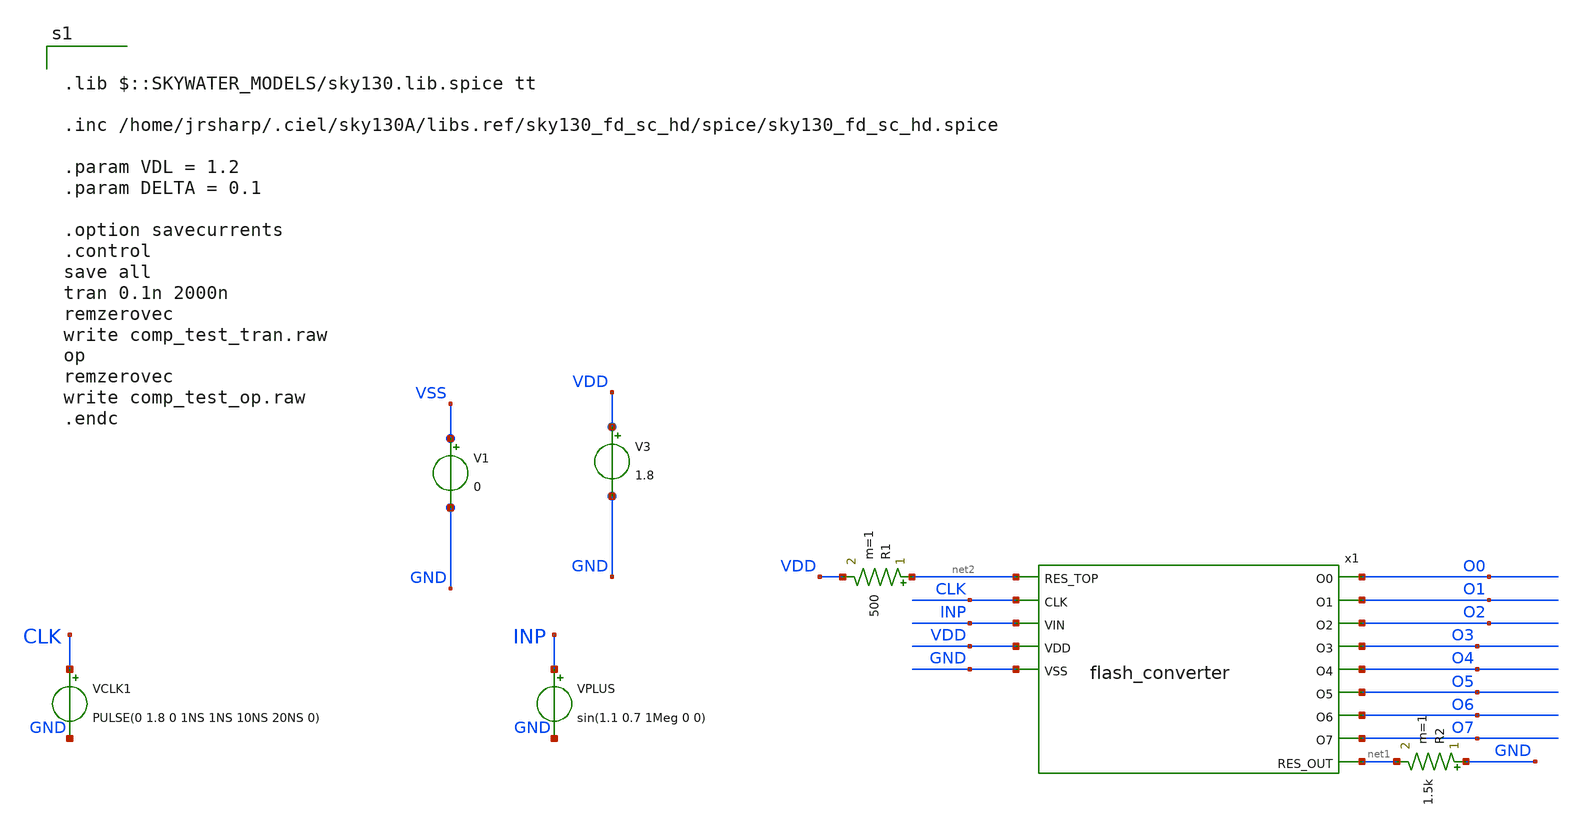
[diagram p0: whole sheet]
** sch_path: xschem/flash_converter/flash_converter_test.sch
**.subckt flash_converter_test
VPLUS INP GND sin(1.1 0.7 1Meg 0 0)
VCLK1 CLK GND PULSE(0 1.8 0 1NS 1NS 10NS 20NS 0)
R1 net2 VDD 500 m=1
R2 GND net1 1.5k m=1
V3 VDD GND 1.8
x1 net2 CLK INP O0 O1 VDD GND O2 O3 O4 O5 O6 O7 net1 flash_converter
V1 VSS GND 0
**** begin user architecture code

.lib $::SKYWATER_MODELS/sky130.lib.spice tt

.inc /home/jrsharp/.ciel/sky130A/libs.ref/sky130_fd_sc_hd/spice/sky130_fd_sc_hd.spice

.param VDL = 1.2
.param DELTA = 0.1

.option savecurrents
.control
save all
tran 0.1n 2000n
remzerovec
write comp_test_tran.raw
op
remzerovec
write comp_test_op.raw
.endc



**** end user architecture code
**.ends

* expanding   symbol:  flash_converter.sym # of pins=14
** sym_path: xschem/flash_converter/flash_converter.sym
** sch_path: xschem/flash_converter/flash_converter.sch
.subckt flash_converter RES_TOP CLK VIN O0 O1 VDD VSS O2 O3 O4 O5 O6 O7 RES_OUT
*.ipin VIN
*.ipin RES_TOP
*.opin RES_OUT
*.opin O0
*.opin O1
*.opin O2
*.opin O3
*.opin O4
*.opin O5
*.opin O6
*.opin O7
*.ipin CLK
*.ipin VDD
*.ipin VSS
x1 CLK VIN RES_TOP VDD O0 VSS high_speed_comp_top
x2 CLK VIN net1 VDD O1 VSS high_speed_comp_top
x3 CLK VIN net2 VDD O2 VSS high_speed_comp_top
x4 CLK VIN net3 VDD O3 VSS high_speed_comp_top
x5 CLK VIN net4 VDD O4 VSS high_speed_comp_top
x6 CLK VIN net5 VDD O5 VSS high_speed_comp_top
x7 CLK VIN net6 VDD O6 VSS high_speed_comp_top
x8 CLK VIN net7 VDD O7 VSS high_speed_comp_top
XR1 net1 RES_TOP VSS sky130_fd_pr__res_high_po_1p41 L=1.41 mult=1 m=1
XR2 net2 net1 VSS sky130_fd_pr__res_high_po_1p41 L=1.41 mult=1 m=1
XR3 net3 net2 VSS sky130_fd_pr__res_high_po_1p41 L=1.41 mult=1 m=1
XR4 net4 net3 VSS sky130_fd_pr__res_high_po_1p41 L=1.41 mult=1 m=1
XR5 net5 net4 VSS sky130_fd_pr__res_high_po_1p41 L=1.41 mult=1 m=1
XR6 net6 net5 VSS sky130_fd_pr__res_high_po_1p41 L=1.41 mult=1 m=1
XR7 net7 net6 VSS sky130_fd_pr__res_high_po_1p41 L=1.41 mult=1 m=1
XR8 RES_OUT net7 VSS sky130_fd_pr__res_high_po_1p41 L=1.41 mult=1 m=1
XR9 VSS VSS VSS sky130_fd_pr__res_high_po_1p41 L=1.41 mult=1 m=1
XR10 VSS VSS VSS sky130_fd_pr__res_high_po_1p41 L=1.41 mult=1 m=1
XR11 VSS VSS VSS sky130_fd_pr__res_high_po_1p41 L=1.41 mult=1 m=1
XR12 VSS VSS VSS sky130_fd_pr__res_high_po_1p41 L=1.41 mult=1 m=1
.ends


* expanding   symbol:  high_speed_comp_top.sym # of pins=6
** sym_path: xschem/flash_converter/high_speed_comp_top.sym
** sch_path: xschem/flash_converter/high_speed_comp_top.sch
.subckt high_speed_comp_top CLK VINP VINN VDD COMP_OUT VSS
*.ipin VINP
*.ipin VINN
*.ipin CLK
*.opin COMP_OUT
*.ipin VDD
*.ipin VSS
x1 VDD CLK_PRIME net1 net2 VSS VINP VINN strong_arm_latch
x2 VDD net1 net2 VOUT VSS post_amplifier
x3 CLK VOUT VSS VSS VDD VDD COMP_OUT sky130_fd_sc_hd__dfxtp_2
x4 CLK VSS VSS VDD VDD CLK_PRIME sky130_fd_sc_hd__clkinv_4
x5 VSS VSS VDD VDD sky130_fd_sc_hd__decap_3
x7 VSS VSS VDD VDD sky130_fd_sc_hd__decap_3
x9 VSS VDD sky130_fd_sc_hd__tapvpwrvgnd_1
x6 VSS VDD sky130_fd_sc_hd__tapvpwrvgnd_1
x8 VSS VDD sky130_fd_sc_hd__tapvpwrvgnd_1
.ends


* expanding   symbol:  strong_arm_latch.sym # of pins=7
** sym_path: xschem/flash_converter/strong_arm_latch.sym
** sch_path: xschem/flash_converter/strong_arm_latch.sch
.subckt strong_arm_latch VDD CLK VOUT_PLUS VOUT_MINUS VSS VINP VINN
*.ipin VSS
*.ipin VDD
*.ipin CLK
*.ipin VINP
*.ipin VINN
*.opin VOUT_MINUS
*.opin VOUT_PLUS
XM1 net2 VINP net1 VSS sky130_fd_pr__nfet_01v8_lvt L=1 W=5 nf=1 ad='int((nf+1)/2) * W/nf * 0.29' as='int((nf+2)/2) * W/nf * 0.29'
+ pd='2*int((nf+1)/2) * (W/nf + 0.29)' ps='2*int((nf+2)/2) * (W/nf + 0.29)' nrd='0.29 / W' nrs='0.29 / W'
+ sa=0 sb=0 sd=0 mult=1 m=1
XM2 net3 VINN net1 VSS sky130_fd_pr__nfet_01v8_lvt L=1 W=5 nf=1 ad='int((nf+1)/2) * W/nf * 0.29' as='int((nf+2)/2) * W/nf * 0.29'
+ pd='2*int((nf+1)/2) * (W/nf + 0.29)' ps='2*int((nf+2)/2) * (W/nf + 0.29)' nrd='0.29 / W' nrs='0.29 / W'
+ sa=0 sb=0 sd=0 mult=1 m=1
XM3 net1 CLK VSS VSS sky130_fd_pr__nfet_01v8_lvt L=1 W=5 nf=1 ad='int((nf+1)/2) * W/nf * 0.29' as='int((nf+2)/2) * W/nf * 0.29'
+ pd='2*int((nf+1)/2) * (W/nf + 0.29)' ps='2*int((nf+2)/2) * (W/nf + 0.29)' nrd='0.29 / W' nrs='0.29 / W'
+ sa=0 sb=0 sd=0 mult=1 m=1
XM4 VOUT_PLUS VOUT_MINUS net2 VSS sky130_fd_pr__nfet_01v8 L=0.15 W=1 nf=1 ad='int((nf+1)/2) * W/nf * 0.29'
+ as='int((nf+2)/2) * W/nf * 0.29' pd='2*int((nf+1)/2) * (W/nf + 0.29)' ps='2*int((nf+2)/2) * (W/nf + 0.29)'
+ nrd='0.29 / W' nrs='0.29 / W' sa=0 sb=0 sd=0 mult=1 m=1
XM5 VOUT_MINUS VOUT_PLUS net3 VSS sky130_fd_pr__nfet_01v8 L=0.15 W=1 nf=1 ad='int((nf+1)/2) * W/nf * 0.29'
+ as='int((nf+2)/2) * W/nf * 0.29' pd='2*int((nf+1)/2) * (W/nf + 0.29)' ps='2*int((nf+2)/2) * (W/nf + 0.29)'
+ nrd='0.29 / W' nrs='0.29 / W' sa=0 sb=0 sd=0 mult=1 m=1
XM6 VOUT_PLUS VOUT_MINUS VDD VDD sky130_fd_pr__pfet_01v8 L=0.15 W=1 nf=1 ad='int((nf+1)/2) * W/nf * 0.29'
+ as='int((nf+2)/2) * W/nf * 0.29' pd='2*int((nf+1)/2) * (W/nf + 0.29)' ps='2*int((nf+2)/2) * (W/nf + 0.29)'
+ nrd='0.29 / W' nrs='0.29 / W' sa=0 sb=0 sd=0 mult=1 m=1
XM7 VOUT_MINUS VOUT_PLUS VDD VDD sky130_fd_pr__pfet_01v8 L=0.15 W=1 nf=1 ad='int((nf+1)/2) * W/nf * 0.29'
+ as='int((nf+2)/2) * W/nf * 0.29' pd='2*int((nf+1)/2) * (W/nf + 0.29)' ps='2*int((nf+2)/2) * (W/nf + 0.29)'
+ nrd='0.29 / W' nrs='0.29 / W' sa=0 sb=0 sd=0 mult=1 m=1
XM8 VOUT_PLUS CLK VDD VDD sky130_fd_pr__pfet_01v8 L=0.15 W=10 nf=1 ad='int((nf+1)/2) * W/nf * 0.29' as='int((nf+2)/2) * W/nf * 0.29'
+ pd='2*int((nf+1)/2) * (W/nf + 0.29)' ps='2*int((nf+2)/2) * (W/nf + 0.29)' nrd='0.29 / W' nrs='0.29 / W'
+ sa=0 sb=0 sd=0 mult=1 m=1
XM9 net2 CLK VDD VDD sky130_fd_pr__pfet_01v8 L=0.15 W=10 nf=1 ad='int((nf+1)/2) * W/nf * 0.29' as='int((nf+2)/2) * W/nf * 0.29'
+ pd='2*int((nf+1)/2) * (W/nf + 0.29)' ps='2*int((nf+2)/2) * (W/nf + 0.29)' nrd='0.29 / W' nrs='0.29 / W'
+ sa=0 sb=0 sd=0 mult=1 m=1
XM10 VOUT_MINUS CLK VDD VDD sky130_fd_pr__pfet_01v8 L=0.15 W=10 nf=1 ad='int((nf+1)/2) * W/nf * 0.29'
+ as='int((nf+2)/2) * W/nf * 0.29' pd='2*int((nf+1)/2) * (W/nf + 0.29)' ps='2*int((nf+2)/2) * (W/nf + 0.29)'
+ nrd='0.29 / W' nrs='0.29 / W' sa=0 sb=0 sd=0 mult=1 m=1
XM11 net3 CLK VDD VDD sky130_fd_pr__pfet_01v8 L=0.15 W=10 nf=1 ad='int((nf+1)/2) * W/nf * 0.29' as='int((nf+2)/2) * W/nf * 0.29'
+ pd='2*int((nf+1)/2) * (W/nf + 0.29)' ps='2*int((nf+2)/2) * (W/nf + 0.29)' nrd='0.29 / W' nrs='0.29 / W'
+ sa=0 sb=0 sd=0 mult=1 m=1
.ends


* expanding   symbol:  post_amplifier.sym # of pins=5
** sym_path: xschem/flash_converter/post_amplifier.sym
** sch_path: xschem/flash_converter/post_amplifier.sch
.subckt post_amplifier VDD VLAT_PLUS VLAT_MINUS VOUT VSS
*.ipin VLAT_PLUS
*.ipin VLAT_MINUS
*.ipin VDD
*.ipin VSS
*.opin VOUT
XM1 net1 VLAT_PLUS net4 VSS sky130_fd_pr__nfet_01v8 L=0.15 W=1 nf=1 ad='int((nf+1)/2) * W/nf * 0.29'
+ as='int((nf+2)/2) * W/nf * 0.29' pd='2*int((nf+1)/2) * (W/nf + 0.29)' ps='2*int((nf+2)/2) * (W/nf + 0.29)'
+ nrd='0.29 / W' nrs='0.29 / W' sa=0 sb=0 sd=0 mult=1 m=1
XM2 net3 VLAT_MINUS net4 VSS sky130_fd_pr__nfet_01v8 L=0.15 W=1 nf=1 ad='int((nf+1)/2) * W/nf * 0.29'
+ as='int((nf+2)/2) * W/nf * 0.29' pd='2*int((nf+1)/2) * (W/nf + 0.29)' ps='2*int((nf+2)/2) * (W/nf + 0.29)'
+ nrd='0.29 / W' nrs='0.29 / W' sa=0 sb=0 sd=0 mult=1 m=1
XM3 net4 net1 VSS VSS sky130_fd_pr__nfet_01v8 L=0.15 W=1 nf=1 ad='int((nf+1)/2) * W/nf * 0.29' as='int((nf+2)/2) * W/nf * 0.29'
+ pd='2*int((nf+1)/2) * (W/nf + 0.29)' ps='2*int((nf+2)/2) * (W/nf + 0.29)' nrd='0.29 / W' nrs='0.29 / W'
+ sa=0 sb=0 sd=0 mult=1 m=1
XM4 net1 VLAT_PLUS net2 VDD sky130_fd_pr__pfet_01v8 L=0.15 W=1 nf=1 ad='int((nf+1)/2) * W/nf * 0.29'
+ as='int((nf+2)/2) * W/nf * 0.29' pd='2*int((nf+1)/2) * (W/nf + 0.29)' ps='2*int((nf+2)/2) * (W/nf + 0.29)'
+ nrd='0.29 / W' nrs='0.29 / W' sa=0 sb=0 sd=0 mult=1 m=1
XM5 net3 VLAT_MINUS net2 VDD sky130_fd_pr__pfet_01v8 L=0.15 W=1 nf=1 ad='int((nf+1)/2) * W/nf * 0.29'
+ as='int((nf+2)/2) * W/nf * 0.29' pd='2*int((nf+1)/2) * (W/nf + 0.29)' ps='2*int((nf+2)/2) * (W/nf + 0.29)'
+ nrd='0.29 / W' nrs='0.29 / W' sa=0 sb=0 sd=0 mult=1 m=1
XM6 net2 net1 VDD VDD sky130_fd_pr__pfet_01v8 L=0.15 W=1 nf=1 ad='int((nf+1)/2) * W/nf * 0.29' as='int((nf+2)/2) * W/nf * 0.29'
+ pd='2*int((nf+1)/2) * (W/nf + 0.29)' ps='2*int((nf+2)/2) * (W/nf + 0.29)' nrd='0.29 / W' nrs='0.29 / W'
+ sa=0 sb=0 sd=0 mult=1 m=1
XM7 VOUT net3 VSS VSS sky130_fd_pr__nfet_01v8 L=0.15 W=1 nf=1 ad='int((nf+1)/2) * W/nf * 0.29' as='int((nf+2)/2) * W/nf * 0.29'
+ pd='2*int((nf+1)/2) * (W/nf + 0.29)' ps='2*int((nf+2)/2) * (W/nf + 0.29)' nrd='0.29 / W' nrs='0.29 / W'
+ sa=0 sb=0 sd=0 mult=1 m=1
XM8 VOUT net3 VDD VDD sky130_fd_pr__pfet_01v8 L=0.15 W=1 nf=1 ad='int((nf+1)/2) * W/nf * 0.29' as='int((nf+2)/2) * W/nf * 0.29'
+ pd='2*int((nf+1)/2) * (W/nf + 0.29)' ps='2*int((nf+2)/2) * (W/nf + 0.29)' nrd='0.29 / W' nrs='0.29 / W'
+ sa=0 sb=0 sd=0 mult=1 m=1
.ends

.GLOBAL VSS
.end
